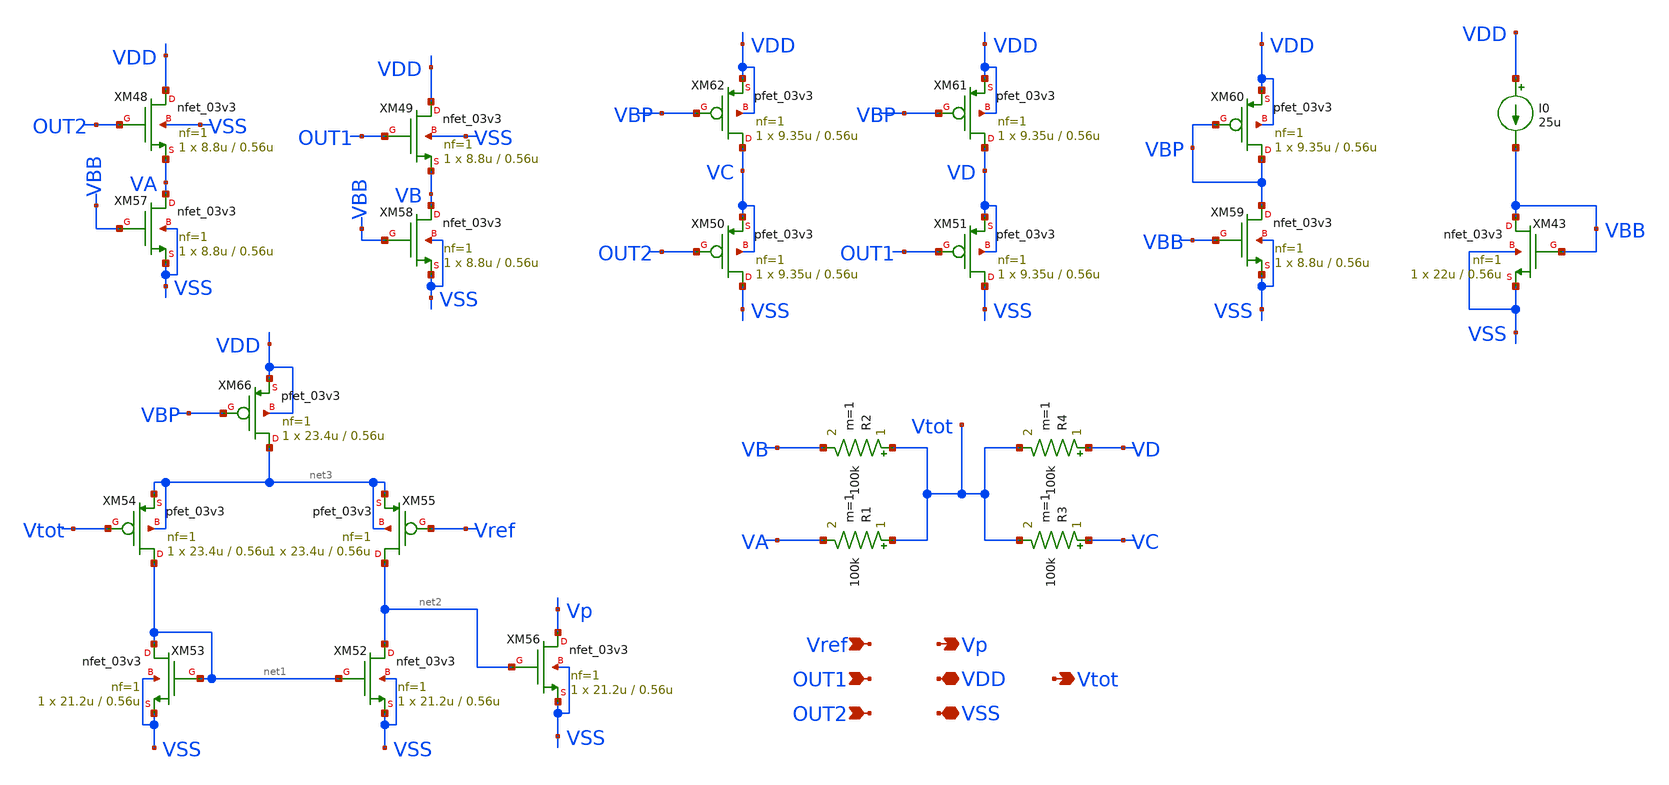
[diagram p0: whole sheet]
** sch_path: SCOP_INPUT_AND_MUX_PAKISTAN_03/Xschem/Others/CM_Extraction.sch
**.subckt CM_Extraction Vref OUT1 OUT2 Vp VDD VSS Vtot
*.ipin Vref
*.ipin OUT1
*.ipin OUT2
*.opin Vp
*.iopin VDD
*.iopin VSS
*.opin Vtot
R2 Vtot VB 100k m=1
R1 Vtot VA 100k m=1
R4 VD Vtot 100k m=1
R3 VC Vtot 100k m=1
XM50 VSS OUT2 VC VC pfet_03v3 L=0.56u W=9.35u nf=1 ad='int((nf+1)/2) * W/nf * 0.18u' as='int((nf+2)/2) * W/nf * 0.18u'
+ pd='2*int((nf+1)/2) * (W/nf + 0.18u)' ps='2*int((nf+2)/2) * (W/nf + 0.18u)' nrd='0.18u / W' nrs='0.18u / W'
+ sa=0 sb=0 sd=0 m=1
XM51 VSS OUT1 VD VD pfet_03v3 L=0.56u W=9.35u nf=1 ad='int((nf+1)/2) * W/nf * 0.18u' as='int((nf+2)/2) * W/nf * 0.18u'
+ pd='2*int((nf+1)/2) * (W/nf + 0.18u)' ps='2*int((nf+2)/2) * (W/nf + 0.18u)' nrd='0.18u / W' nrs='0.18u / W'
+ sa=0 sb=0 sd=0 m=1
XM61 VD VBP VDD VDD pfet_03v3 L=0.56u W=9.35u nf=1 ad='int((nf+1)/2) * W/nf * 0.18u' as='int((nf+2)/2) * W/nf * 0.18u'
+ pd='2*int((nf+1)/2) * (W/nf + 0.18u)' ps='2*int((nf+2)/2) * (W/nf + 0.18u)' nrd='0.18u / W' nrs='0.18u / W'
+ sa=0 sb=0 sd=0 m=1
XM62 VC VBP VDD VDD pfet_03v3 L=0.56u W=9.35u nf=1 ad='int((nf+1)/2) * W/nf * 0.18u' as='int((nf+2)/2) * W/nf * 0.18u'
+ pd='2*int((nf+1)/2) * (W/nf + 0.18u)' ps='2*int((nf+2)/2) * (W/nf + 0.18u)' nrd='0.18u / W' nrs='0.18u / W'
+ sa=0 sb=0 sd=0 m=1
XM59 VBP VBB VSS VSS nfet_03v3 L=0.56u W=8.8u nf=1 ad='int((nf+1)/2) * W/nf * 0.18u' as='int((nf+2)/2) * W/nf * 0.18u'
+ pd='2*int((nf+1)/2) * (W/nf + 0.18u)' ps='2*int((nf+2)/2) * (W/nf + 0.18u)' nrd='0.18u / W' nrs='0.18u / W'
+ sa=0 sb=0 sd=0 m=1
XM60 VBP VBP VDD VDD pfet_03v3 L=0.56u W=9.35u nf=1 ad='int((nf+1)/2) * W/nf * 0.18u' as='int((nf+2)/2) * W/nf * 0.18u'
+ pd='2*int((nf+1)/2) * (W/nf + 0.18u)' ps='2*int((nf+2)/2) * (W/nf + 0.18u)' nrd='0.18u / W' nrs='0.18u / W'
+ sa=0 sb=0 sd=0 m=1
XM49 VDD OUT1 VB VSS nfet_03v3 L=0.56u W=8.8u nf=1 ad='int((nf+1)/2) * W/nf * 0.18u' as='int((nf+2)/2) * W/nf * 0.18u'
+ pd='2*int((nf+1)/2) * (W/nf + 0.18u)' ps='2*int((nf+2)/2) * (W/nf + 0.18u)' nrd='0.18u / W' nrs='0.18u / W'
+ sa=0 sb=0 sd=0 m=1
XM58 VB VBB VSS VSS nfet_03v3 L=0.56u W=8.8u nf=1 ad='int((nf+1)/2) * W/nf * 0.18u' as='int((nf+2)/2) * W/nf * 0.18u'
+ pd='2*int((nf+1)/2) * (W/nf + 0.18u)' ps='2*int((nf+2)/2) * (W/nf + 0.18u)' nrd='0.18u / W' nrs='0.18u / W'
+ sa=0 sb=0 sd=0 m=1
XM48 VDD OUT2 VA VSS nfet_03v3 L=0.56u W=8.8u nf=1 ad='int((nf+1)/2) * W/nf * 0.18u' as='int((nf+2)/2) * W/nf * 0.18u'
+ pd='2*int((nf+1)/2) * (W/nf + 0.18u)' ps='2*int((nf+2)/2) * (W/nf + 0.18u)' nrd='0.18u / W' nrs='0.18u / W'
+ sa=0 sb=0 sd=0 m=1
XM57 VA VBB VSS VSS nfet_03v3 L=0.56u W=8.8u nf=1 ad='int((nf+1)/2) * W/nf * 0.18u' as='int((nf+2)/2) * W/nf * 0.18u'
+ pd='2*int((nf+1)/2) * (W/nf + 0.18u)' ps='2*int((nf+2)/2) * (W/nf + 0.18u)' nrd='0.18u / W' nrs='0.18u / W'
+ sa=0 sb=0 sd=0 m=1
XM52 net2 net1 VSS VSS nfet_03v3 L=0.56u W=21.2u nf=1 ad='int((nf+1)/2) * W/nf * 0.18u' as='int((nf+2)/2) * W/nf * 0.18u'
+ pd='2*int((nf+1)/2) * (W/nf + 0.18u)' ps='2*int((nf+2)/2) * (W/nf + 0.18u)' nrd='0.18u / W' nrs='0.18u / W'
+ sa=0 sb=0 sd=0 m=1
XM53 net1 net1 VSS VSS nfet_03v3 L=0.56u W=21.2u nf=1 ad='int((nf+1)/2) * W/nf * 0.18u' as='int((nf+2)/2) * W/nf * 0.18u'
+ pd='2*int((nf+1)/2) * (W/nf + 0.18u)' ps='2*int((nf+2)/2) * (W/nf + 0.18u)' nrd='0.18u / W' nrs='0.18u / W'
+ sa=0 sb=0 sd=0 m=1
XM54 net1 Vtot net3 net3 pfet_03v3 L=0.56u W=23.4u nf=1 ad='int((nf+1)/2) * W/nf * 0.18u' as='int((nf+2)/2) * W/nf * 0.18u'
+ pd='2*int((nf+1)/2) * (W/nf + 0.18u)' ps='2*int((nf+2)/2) * (W/nf + 0.18u)' nrd='0.18u / W' nrs='0.18u / W'
+ sa=0 sb=0 sd=0 m=1
XM55 net2 Vref net3 net3 pfet_03v3 L=0.56u W=23.4u nf=1 ad='int((nf+1)/2) * W/nf * 0.18u' as='int((nf+2)/2) * W/nf * 0.18u'
+ pd='2*int((nf+1)/2) * (W/nf + 0.18u)' ps='2*int((nf+2)/2) * (W/nf + 0.18u)' nrd='0.18u / W' nrs='0.18u / W'
+ sa=0 sb=0 sd=0 m=1
XM56 Vp net2 VSS VSS nfet_03v3 L=0.56u W=21.2u nf=1 ad='int((nf+1)/2) * W/nf * 0.18u' as='int((nf+2)/2) * W/nf * 0.18u'
+ pd='2*int((nf+1)/2) * (W/nf + 0.18u)' ps='2*int((nf+2)/2) * (W/nf + 0.18u)' nrd='0.18u / W' nrs='0.18u / W'
+ sa=0 sb=0 sd=0 m=1
XM66 net3 VBP VDD VDD pfet_03v3 L=0.56u W=23.4u nf=1 ad='int((nf+1)/2) * W/nf * 0.18u' as='int((nf+2)/2) * W/nf * 0.18u'
+ pd='2*int((nf+1)/2) * (W/nf + 0.18u)' ps='2*int((nf+2)/2) * (W/nf + 0.18u)' nrd='0.18u / W' nrs='0.18u / W'
+ sa=0 sb=0 sd=0 m=1
XM43 VBB VBB VSS VSS nfet_03v3 L=0.56u W=22u nf=1 ad='int((nf+1)/2) * W/nf * 0.18u' as='int((nf+2)/2) * W/nf * 0.18u'
+ pd='2*int((nf+1)/2) * (W/nf + 0.18u)' ps='2*int((nf+2)/2) * (W/nf + 0.18u)' nrd='0.18u / W' nrs='0.18u / W'
+ sa=0 sb=0 sd=0 m=1
I0 VDD VBB 25u
**.ends
.end
